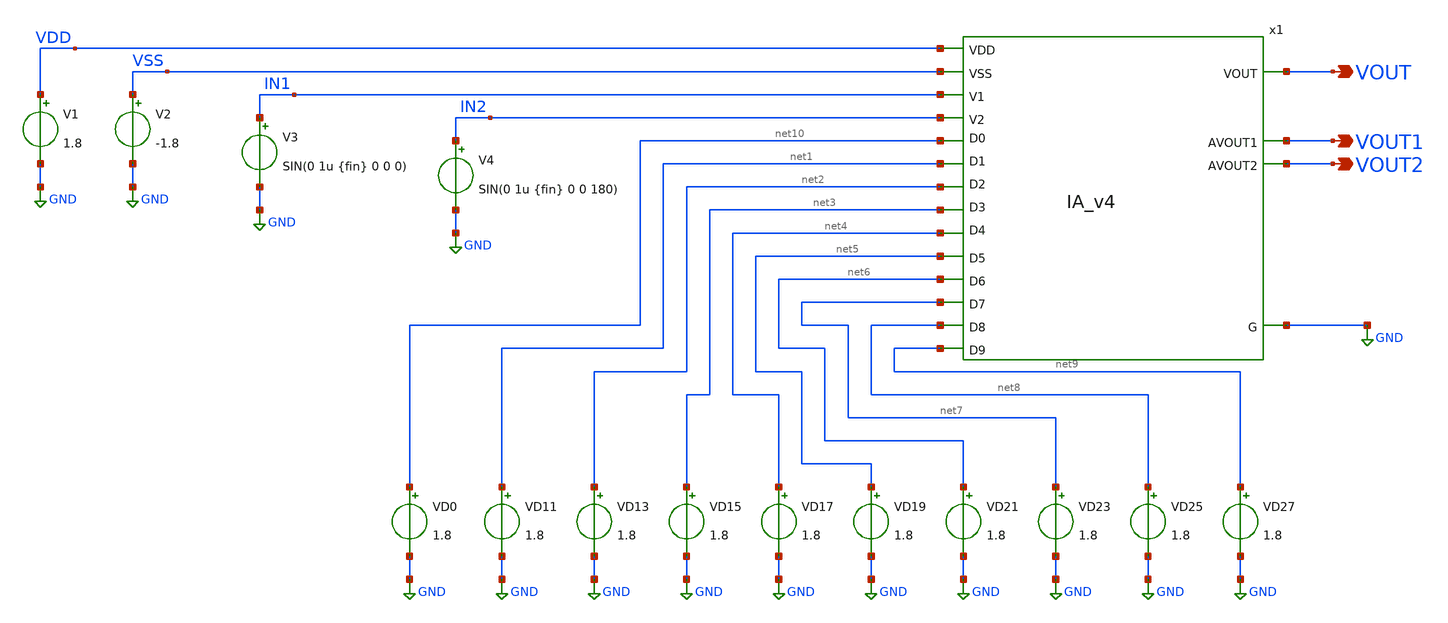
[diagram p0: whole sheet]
** sch_path: xschem/IA_v4_testbench.sch
**.subckt IA_v4_testbench VOUT VOUT1 VOUT2
*.opin VOUT
*.opin VOUT1
*.opin VOUT2
V1 VDD GND 1.8
V2 VSS GND -1.8
V3 IN1 GND SIN(0 1u {fin} 0 0 0)
V4 IN2 GND SIN(0 1u {fin} 0 0 180)
VD0 net10 GND 1.8
VD11 net1 GND 1.8
VD13 net2 GND 1.8
VD15 net3 GND 1.8
VD17 net4 GND 1.8
VD19 net5 GND 1.8
VD21 net6 GND 1.8
VD23 net7 GND 1.8
VD25 net8 GND 1.8
VD27 net9 GND 1.8
x1 VDD VSS GND IN1 IN2 net10 net1 net2 net3 net4 net5 net6 net7 net8 net9 VOUT1 VOUT2 VOUT IA_v4
**** begin user architecture code

*.include /foss/designs/sky130_hcmus_ip__instramp/xschem/layout/IA_v4.pex.spice
.param fin = 10K
.control
save all
tran 0.1u 100u
meas tran minv MIN v(vout)
meas tran maxv MAX v(vout)
let gain = ((abs(maxv)+abs(minv))/(2e-6))
print gain
write IA_v4_testbench.raw
.endc

.lib $::SKYWATER_MODELS/sky130.lib.spice tt
**** end user architecture code
**.ends

* expanding   symbol:  IA_v4.sym # of pins=18
** sym_path: xschem/IA_v4.sym
** sch_path: xschem/IA_v4.sch
.subckt IA_v4 VDD VSS G V1 V2 D0 D1 D2 D3 D4 D5 D6 D7 D8 D9 AVOUT1 AVOUT2 VOUT
*.opin VOUT
*.iopin G
*.ipin VDD
*.ipin VSS
*.ipin V1
*.ipin V2
*.ipin D4
*.ipin D3
*.ipin D2
*.ipin D1
*.ipin D0
*.ipin D9
*.ipin D8
*.ipin D7
*.ipin D6
*.ipin D5
*.opin AVOUT1
*.opin AVOUT2
x4 VDD VSS V2 net3 AVOUT1 opamp
x5 VDD VSS V1 net4 AVOUT2 opamp
x6 VDD VSS net2 net1 VOUT opamp
x1 G net3 AVOUT1 D0 D1 D2 D3 D4 VDD RB_array_20
x2 G net4 AVOUT2 D0 D1 D2 D3 D4 VDD RB_array_20
x3 G net1 VOUT D5 D6 D7 D8 D9 VDD RB_array_20
x7 G net2 G D5 D6 D7 D8 D9 VDD RB_array_20
XR4 net5 net1 G sky130_fd_pr__res_high_po_0p69 L=12.22 mult=64 m=64
XR1 net3 net4 G sky130_fd_pr__res_high_po_0p69 L=12.22 mult=64 m=64
XR2 net2 net6 G sky130_fd_pr__res_high_po_0p69 L=12.22 mult=64 m=64
x8 VDD VSS AVOUT1 net5 net5 opamp
x9 VDD VSS AVOUT2 net6 net6 opamp
.ends


* expanding   symbol:  ../xschem/opamp.sym # of pins=5
** sym_path: xschem/opamp.sym
** sch_path: xschem/opamp.sch
.subckt opamp VDD VSS V1 V2 VOUT
*.ipin VSS
*.ipin VDD
*.ipin V2
*.ipin V1
*.opin VOUT
XM2 net5 V2 net1 VSS sky130_fd_pr__nfet_01v8 L=1 W=8.5 nf=1 ad='int((nf+1)/2) * W/nf * 0.29' as='int((nf+2)/2) * W/nf * 0.29'
+ pd='2*int((nf+1)/2) * (W/nf + 0.29)' ps='2*int((nf+2)/2) * (W/nf + 0.29)' nrd='0.29 / W' nrs='0.29 / W'
+ sa=0 sb=0 sd=0 mult=1 m=1
XM1 net6 net5 VDD VDD sky130_fd_pr__pfet_01v8 L=1 W=41 nf=1 ad='int((nf+1)/2) * W/nf * 0.29' as='int((nf+2)/2) * W/nf * 0.29'
+ pd='2*int((nf+1)/2) * (W/nf + 0.29)' ps='2*int((nf+2)/2) * (W/nf + 0.29)' nrd='0.29 / W' nrs='0.29 / W'
+ sa=0 sb=0 sd=0 mult=1 m=1
XM4 net6 V1 net1 VSS sky130_fd_pr__nfet_01v8 L=1 W=8.5 nf=1 ad='int((nf+1)/2) * W/nf * 0.29' as='int((nf+2)/2) * W/nf * 0.29'
+ pd='2*int((nf+1)/2) * (W/nf + 0.29)' ps='2*int((nf+2)/2) * (W/nf + 0.29)' nrd='0.29 / W' nrs='0.29 / W'
+ sa=0 sb=0 sd=0 mult=1 m=1
XM5 net1 net4 VSS VSS sky130_fd_pr__nfet_01v8 L=1 W=20 nf=1 ad='int((nf+1)/2) * W/nf * 0.29' as='int((nf+2)/2) * W/nf * 0.29'
+ pd='2*int((nf+1)/2) * (W/nf + 0.29)' ps='2*int((nf+2)/2) * (W/nf + 0.29)' nrd='0.29 / W' nrs='0.29 / W'
+ sa=0 sb=0 sd=0 mult=1 m=1
XM6 VOUT net4 VSS VSS sky130_fd_pr__nfet_01v8 L=1 W=19 nf=1 ad='int((nf+1)/2) * W/nf * 0.29' as='int((nf+2)/2) * W/nf * 0.29'
+ pd='2*int((nf+1)/2) * (W/nf + 0.29)' ps='2*int((nf+2)/2) * (W/nf + 0.29)' nrd='0.29 / W' nrs='0.29 / W'
+ sa=0 sb=0 sd=0 mult=1 m=1
XM7 net4 net4 VSS VSS sky130_fd_pr__nfet_01v8 L=1 W=20 nf=1 ad='int((nf+1)/2) * W/nf * 0.29' as='int((nf+2)/2) * W/nf * 0.29'
+ pd='2*int((nf+1)/2) * (W/nf + 0.29)' ps='2*int((nf+2)/2) * (W/nf + 0.29)' nrd='0.29 / W' nrs='0.29 / W'
+ sa=0 sb=0 sd=0 mult=1 m=1
XM3 net5 net5 VDD VDD sky130_fd_pr__pfet_01v8 L=1 W=41 nf=1 ad='int((nf+1)/2) * W/nf * 0.29' as='int((nf+2)/2) * W/nf * 0.29'
+ pd='2*int((nf+1)/2) * (W/nf + 0.29)' ps='2*int((nf+2)/2) * (W/nf + 0.29)' nrd='0.29 / W' nrs='0.29 / W'
+ sa=0 sb=0 sd=0 mult=1 m=1
XM8 VOUT net6 VDD VDD sky130_fd_pr__pfet_01v8 L=1 W=40 nf=1 ad='int((nf+1)/2) * W/nf * 0.29' as='int((nf+2)/2) * W/nf * 0.29'
+ pd='2*int((nf+1)/2) * (W/nf + 0.29)' ps='2*int((nf+2)/2) * (W/nf + 0.29)' nrd='0.29 / W' nrs='0.29 / W'
+ sa=0 sb=0 sd=0 mult=2 m=2
XR3 net2 VDD VSS sky130_fd_pr__res_high_po W=1 L=50 mult=1 m=1
XR1 net3 net2 VSS sky130_fd_pr__res_high_po W=1 L=50 mult=1 m=1
XR2 net4 net3 VSS sky130_fd_pr__res_high_po W=1 L=50 mult=1 m=1
XR4 net7 VOUT VSS sky130_fd_pr__res_high_po W=1 L=7 mult=1 m=1
XC1 net7 net6 sky130_fd_pr__cap_mim_m3_1 W=5.55 L=10 MF=20 m=20
.ends


* expanding   symbol:  ../xschem/RB_array_20.sym # of pins=9
** sym_path: xschem/RB_array_20.sym
** sch_path: xschem/RB_array_20.sch
.subckt RB_array_20 VSS R1 R2 D0 D1 D2 D3 D4 VDD
*.ipin VSS
*.iopin R2
*.ipin D0
*.ipin D1
*.ipin D2
*.ipin D3
*.ipin D4
*.iopin R1
*.ipin VDD
XR2 net6 R2 VSS sky130_fd_pr__res_high_po_0p69 L=12.22 mult=1 m=1
XR1 net1 R2 VSS sky130_fd_pr__res_high_po_0p69 L=12.22 mult=1 m=1
XR3 net5 R2 VSS sky130_fd_pr__res_high_po_0p69 L=12.22 mult=2 m=2
XR4 net4 R2 VSS sky130_fd_pr__res_high_po_0p69 L=12.22 mult=4 m=4
XR5 net3 R2 VSS sky130_fd_pr__res_high_po_0p69 L=12.22 mult=8 m=8
XR6 net2 R2 VSS sky130_fd_pr__res_high_po_0p69 L=12.22 mult=16 m=16
XM6 net8 D0 net1 VSS sky130_fd_pr__nfet_g5v0d10v5 L=1 W=4.77 nf=1 ad='int((nf+1)/2) * W/nf * 0.29' as='int((nf+2)/2) * W/nf * 0.29'
+ pd='2*int((nf+1)/2) * (W/nf + 0.29)' ps='2*int((nf+2)/2) * (W/nf + 0.29)' nrd='0.29 / W' nrs='0.29 / W'
+ sa=0 sb=0 sd=0 mult=1 m=1
XM7 net12 D1 net5 VSS sky130_fd_pr__nfet_g5v0d10v5 L=1 W=9.74 nf=2 ad='int((nf+1)/2) * W/nf * 0.29' as='int((nf+2)/2) * W/nf * 0.29'
+ pd='2*int((nf+1)/2) * (W/nf + 0.29)' ps='2*int((nf+2)/2) * (W/nf + 0.29)' nrd='0.29 / W' nrs='0.29 / W'
+ sa=0 sb=0 sd=0 mult=1 m=1
XM8 net9 D2 net4 VSS sky130_fd_pr__nfet_g5v0d10v5 L=1 W=18.60 nf=4 ad='int((nf+1)/2) * W/nf * 0.29' as='int((nf+2)/2) * W/nf * 0.29'
+ pd='2*int((nf+1)/2) * (W/nf + 0.29)' ps='2*int((nf+2)/2) * (W/nf + 0.29)' nrd='0.29 / W' nrs='0.29 / W'
+ sa=0 sb=0 sd=0 mult=1 m=1
XM9 net10 D3 net3 VSS sky130_fd_pr__nfet_g5v0d10v5 L=1 W=35.04 nf=8 ad='int((nf+1)/2) * W/nf * 0.29'
+ as='int((nf+2)/2) * W/nf * 0.29' pd='2*int((nf+1)/2) * (W/nf + 0.29)' ps='2*int((nf+2)/2) * (W/nf + 0.29)'
+ nrd='0.29 / W' nrs='0.29 / W' sa=0 sb=0 sd=0 mult=1 m=1
XM10 net11 D4 net2 VSS sky130_fd_pr__nfet_g5v0d10v5 L=1 W=61.60 nf=14 ad='int((nf+1)/2) * W/nf * 0.29'
+ as='int((nf+2)/2) * W/nf * 0.29' pd='2*int((nf+1)/2) * (W/nf + 0.29)' ps='2*int((nf+2)/2) * (W/nf + 0.29)'
+ nrd='0.29 / W' nrs='0.29 / W' sa=0 sb=0 sd=0 mult=1 m=1
XM11 net7 VDD net6 VSS sky130_fd_pr__nfet_g5v0d10v5 L=1 W=4.77 nf=1 ad='int((nf+1)/2) * W/nf * 0.29'
+ as='int((nf+2)/2) * W/nf * 0.29' pd='2*int((nf+1)/2) * (W/nf + 0.29)' ps='2*int((nf+2)/2) * (W/nf + 0.29)'
+ nrd='0.29 / W' nrs='0.29 / W' sa=0 sb=0 sd=0 mult=1 m=1
Vmeas R1 net7 0
.save i(vmeas)
Vmeas1 R1 net8 0
.save i(vmeas1)
Vmeas2 R1 net12 0
.save i(vmeas2)
Vmeas3 R1 net9 0
.save i(vmeas3)
Vmeas4 R1 net10 0
.save i(vmeas4)
Vmeas5 R1 net11 0
.save i(vmeas5)
.ends

.GLOBAL GND
.end
